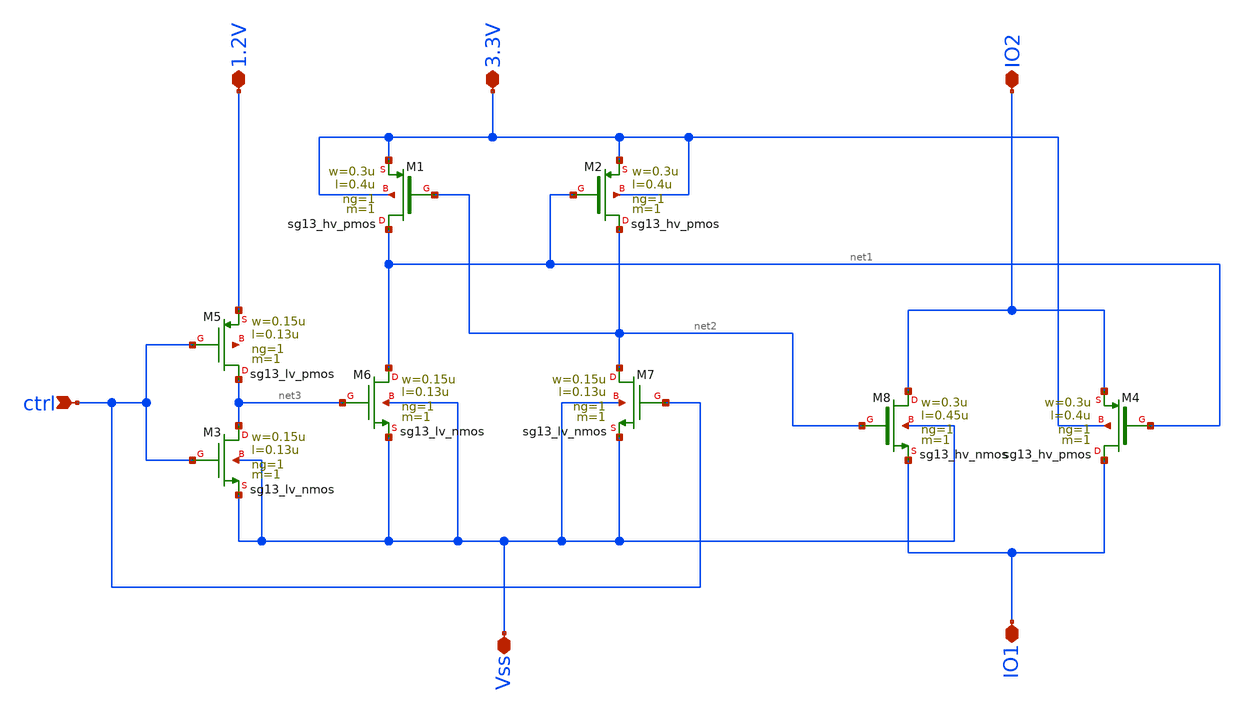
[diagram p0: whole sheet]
** sch_path: design_data/xschem/level_shifter.sch
* Copyright 2025 IHP PDK Authors
**.subckt level_shifter IO1 Vss IO2 3.3V ctrl 1.2V
*.iopin IO1
*.iopin Vss
*.iopin IO2
*.iopin 3.3V
*.ipin ctrl
*.iopin 1.2V
XM2 net2 net1 3.3V 3.3V sg13_hv_pmos w=0.3u l=0.4u ng=1 m=1 mm_ok=1
XM3 net3 ctrl Vss Vss sg13_lv_nmos w=0.15u l=0.13u ng=1 m=1 mm_ok=1
XM5 net3 ctrl 1.2V net4 sg13_lv_pmos w=0.15u l=0.13u ng=1 m=1 mm_ok=1
XM6 net1 net3 Vss Vss sg13_lv_nmos w=0.15u l=0.13u ng=1 m=1 mm_ok=1
XM7 net2 ctrl Vss Vss sg13_lv_nmos w=0.15u l=0.13u ng=1 m=1 mm_ok=1
XM1 net1 net2 3.3V 3.3V sg13_hv_pmos w=0.3u l=0.4u ng=1 m=1 mm_ok=1
XM4 IO1 net1 IO2 3.3V sg13_hv_pmos w=0.3u l=0.4u ng=1 m=1 mm_ok=1
XM8 IO2 net2 IO1 Vss sg13_hv_nmos w=0.3u l=0.45u ng=1 m=1 mm_ok=1
**.ends
.end
